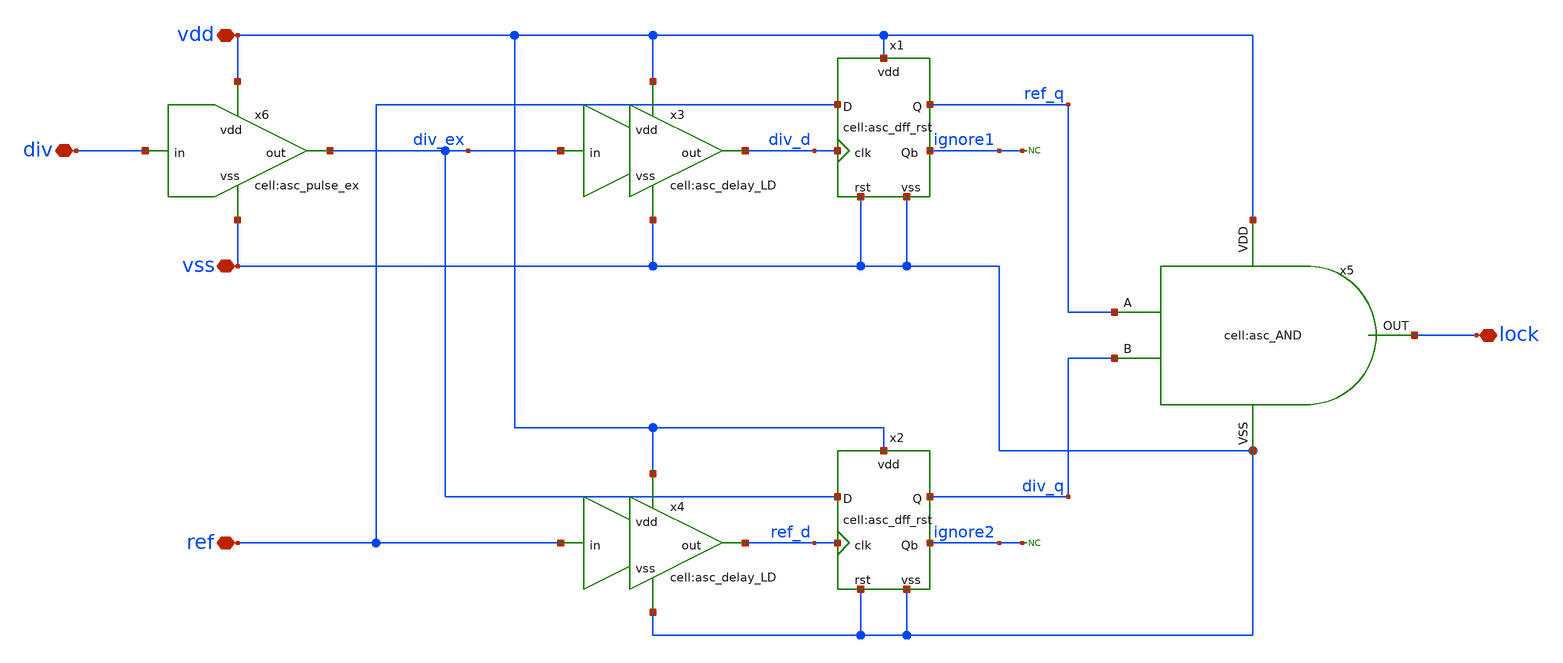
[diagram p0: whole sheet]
** sch_path: designs/libs/core_analog/asc_lock_detector_20250826/asc_lock_detector_20250826.sch
**.subckt asc_lock_detector_20250826 vdd vss div ref lock
*.iopin vdd
*.iopin vss
*.iopin div
*.iopin ref
*.iopin lock
x5 vdd lock ref_q div_q vss asc_AND
* noconn ignore1
* noconn ignore2
x1 div_d ref ignore1 vdd vss ref_q vss asc_dff_rst
x2 ref_d div_ex ignore2 vdd vss div_q vss asc_dff_rst
x3 div_ex vss div_d vdd asc_delay_LD
x4 ref vss ref_d vdd asc_delay_LD
x6 div vss div_ex vdd asc_pulse_ex
**.ends
.end
